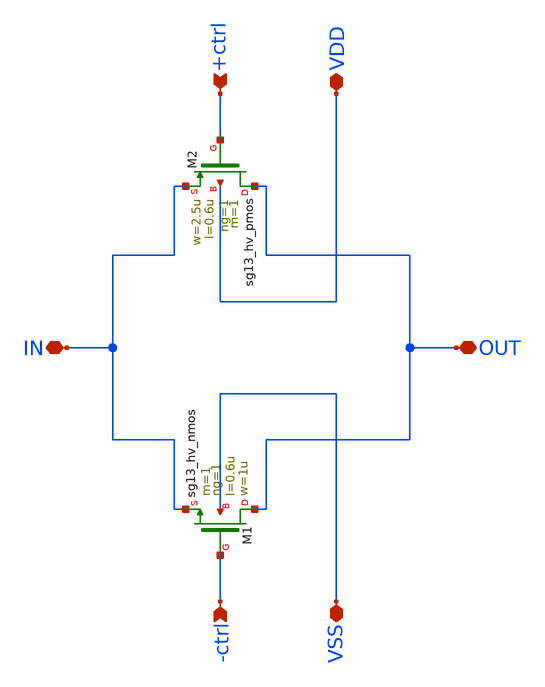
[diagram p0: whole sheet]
** sch_path: real_circuit/sandbox/real_switch.sch
**.subckt real_switch IN OUT VDD VSS +ctrl -ctrl
*.iopin IN
*.iopin OUT
*.iopin VDD
*.iopin VSS
*.ipin +ctrl
*.ipin -ctrl
XM1 OUT -ctrl IN VSS sg13_hv_nmos w=1u l=0.6u ng=1 m=1 mm_ok=1
XM2 OUT +ctrl IN VDD sg13_hv_pmos w=2.5u l=0.6u ng=1 m=1 mm_ok=1
**.ends
.end
